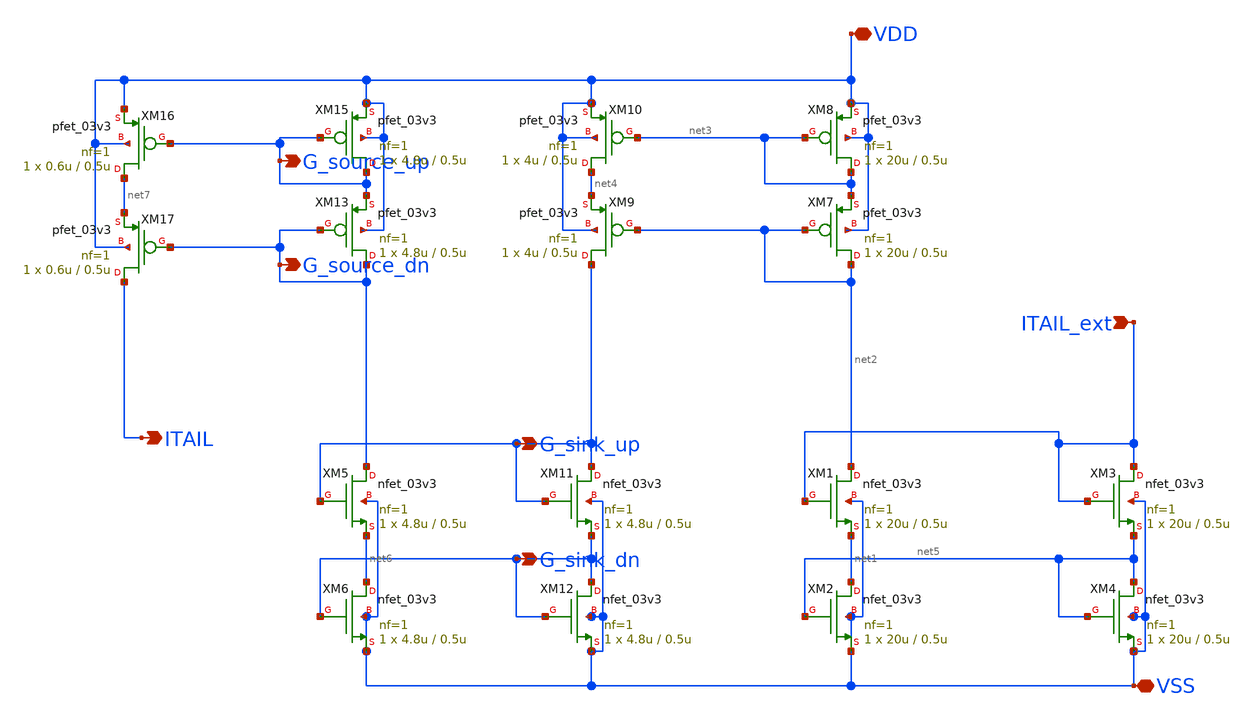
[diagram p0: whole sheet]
** sch_path: DAC_PAKISTAN_01/Pakistan1_Xschem/Current_Mirror_Top_s.sch
**.subckt Current_Mirror_Top_s ITAIL_ext VDD VSS G_source_up G_source_dn G_sink_up G_sink_dn ITAIL
*.ipin ITAIL_ext
*.iopin VDD
*.iopin VSS
*.opin G_source_up
*.opin G_source_dn
*.opin G_sink_up
*.opin G_sink_dn
*.opin ITAIL
XM1 net2 ITAIL_ext net1 VSS nfet_03v3 L=0.5u W=20u nf=1 ad='int((nf+1)/2) * W/nf * 0.18u' as='int((nf+2)/2) * W/nf * 0.18u'
+ pd='2*int((nf+1)/2) * (W/nf + 0.18u)' ps='2*int((nf+2)/2) * (W/nf + 0.18u)' nrd='0.18u / W' nrs='0.18u / W'
+ sa=0 sb=0 sd=0 m=1
XM2 net1 net5 VSS VSS nfet_03v3 L=0.5u W=20u nf=1 ad='int((nf+1)/2) * W/nf * 0.18u' as='int((nf+2)/2) * W/nf * 0.18u'
+ pd='2*int((nf+1)/2) * (W/nf + 0.18u)' ps='2*int((nf+2)/2) * (W/nf + 0.18u)' nrd='0.18u / W' nrs='0.18u / W'
+ sa=0 sb=0 sd=0 m=1
XM7 net2 net2 net3 VDD pfet_03v3 L=0.5u W=20u nf=1 ad='int((nf+1)/2) * W/nf * 0.18u' as='int((nf+2)/2) * W/nf * 0.18u'
+ pd='2*int((nf+1)/2) * (W/nf + 0.18u)' ps='2*int((nf+2)/2) * (W/nf + 0.18u)' nrd='0.18u / W' nrs='0.18u / W'
+ sa=0 sb=0 sd=0 m=1
XM8 net3 net3 VDD VDD pfet_03v3 L=0.5u W=20u nf=1 ad='int((nf+1)/2) * W/nf * 0.18u' as='int((nf+2)/2) * W/nf * 0.18u'
+ pd='2*int((nf+1)/2) * (W/nf + 0.18u)' ps='2*int((nf+2)/2) * (W/nf + 0.18u)' nrd='0.18u / W' nrs='0.18u / W'
+ sa=0 sb=0 sd=0 m=1
XM9 G_sink_up net2 net4 VDD pfet_03v3 L=0.5u W=4u nf=1 ad='int((nf+1)/2) * W/nf * 0.18u' as='int((nf+2)/2) * W/nf * 0.18u'
+ pd='2*int((nf+1)/2) * (W/nf + 0.18u)' ps='2*int((nf+2)/2) * (W/nf + 0.18u)' nrd='0.18u / W' nrs='0.18u / W'
+ sa=0 sb=0 sd=0 m=1
XM10 net4 net3 VDD VDD pfet_03v3 L=0.5u W=4u nf=1 ad='int((nf+1)/2) * W/nf * 0.18u' as='int((nf+2)/2) * W/nf * 0.18u'
+ pd='2*int((nf+1)/2) * (W/nf + 0.18u)' ps='2*int((nf+2)/2) * (W/nf + 0.18u)' nrd='0.18u / W' nrs='0.18u / W'
+ sa=0 sb=0 sd=0 m=1
XM11 G_sink_up G_sink_up G_sink_dn VSS nfet_03v3 L=0.5u W=4.8u nf=1 ad='int((nf+1)/2) * W/nf * 0.18u'
+ as='int((nf+2)/2) * W/nf * 0.18u' pd='2*int((nf+1)/2) * (W/nf + 0.18u)' ps='2*int((nf+2)/2) * (W/nf + 0.18u)'
+ nrd='0.18u / W' nrs='0.18u / W' sa=0 sb=0 sd=0 m=1
XM12 G_sink_dn G_sink_dn VSS VSS nfet_03v3 L=0.5u W=4.8u nf=1 ad='int((nf+1)/2) * W/nf * 0.18u' as='int((nf+2)/2) * W/nf * 0.18u'
+ pd='2*int((nf+1)/2) * (W/nf + 0.18u)' ps='2*int((nf+2)/2) * (W/nf + 0.18u)' nrd='0.18u / W' nrs='0.18u / W'
+ sa=0 sb=0 sd=0 m=1
XM3 ITAIL_ext ITAIL_ext net5 VSS nfet_03v3 L=0.5u W=20u nf=1 ad='int((nf+1)/2) * W/nf * 0.18u' as='int((nf+2)/2) * W/nf * 0.18u'
+ pd='2*int((nf+1)/2) * (W/nf + 0.18u)' ps='2*int((nf+2)/2) * (W/nf + 0.18u)' nrd='0.18u / W' nrs='0.18u / W'
+ sa=0 sb=0 sd=0 m=1
XM4 net5 net5 VSS VSS nfet_03v3 L=0.5u W=20u nf=1 ad='int((nf+1)/2) * W/nf * 0.18u' as='int((nf+2)/2) * W/nf * 0.18u'
+ pd='2*int((nf+1)/2) * (W/nf + 0.18u)' ps='2*int((nf+2)/2) * (W/nf + 0.18u)' nrd='0.18u / W' nrs='0.18u / W'
+ sa=0 sb=0 sd=0 m=1
XM5 G_source_dn G_sink_up net6 VSS nfet_03v3 L=0.5u W=4.8u nf=1 ad='int((nf+1)/2) * W/nf * 0.18u' as='int((nf+2)/2) * W/nf * 0.18u'
+ pd='2*int((nf+1)/2) * (W/nf + 0.18u)' ps='2*int((nf+2)/2) * (W/nf + 0.18u)' nrd='0.18u / W' nrs='0.18u / W'
+ sa=0 sb=0 sd=0 m=1
XM6 net6 G_sink_dn VSS VSS nfet_03v3 L=0.5u W=4.8u nf=1 ad='int((nf+1)/2) * W/nf * 0.18u' as='int((nf+2)/2) * W/nf * 0.18u'
+ pd='2*int((nf+1)/2) * (W/nf + 0.18u)' ps='2*int((nf+2)/2) * (W/nf + 0.18u)' nrd='0.18u / W' nrs='0.18u / W'
+ sa=0 sb=0 sd=0 m=1
XM13 G_source_dn G_source_dn G_source_up VDD pfet_03v3 L=0.5u W=4.8u nf=1 ad='int((nf+1)/2) * W/nf * 0.18u'
+ as='int((nf+2)/2) * W/nf * 0.18u' pd='2*int((nf+1)/2) * (W/nf + 0.18u)' ps='2*int((nf+2)/2) * (W/nf + 0.18u)'
+ nrd='0.18u / W' nrs='0.18u / W' sa=0 sb=0 sd=0 m=1
XM15 G_source_up G_source_up VDD VDD pfet_03v3 L=0.5u W=4.8u nf=1 ad='int((nf+1)/2) * W/nf * 0.18u' as='int((nf+2)/2) * W/nf * 0.18u'
+ pd='2*int((nf+1)/2) * (W/nf + 0.18u)' ps='2*int((nf+2)/2) * (W/nf + 0.18u)' nrd='0.18u / W' nrs='0.18u / W'
+ sa=0 sb=0 sd=0 m=1
XM16 net7 G_source_up VDD VDD pfet_03v3 L=0.5u W=0.6u nf=1 ad='int((nf+1)/2) * W/nf * 0.18u' as='int((nf+2)/2) * W/nf * 0.18u'
+ pd='2*int((nf+1)/2) * (W/nf + 0.18u)' ps='2*int((nf+2)/2) * (W/nf + 0.18u)' nrd='0.18u / W' nrs='0.18u / W'
+ sa=0 sb=0 sd=0 m=1
XM17 ITAIL G_source_dn net7 VDD pfet_03v3 L=0.5u W=0.6u nf=1 ad='int((nf+1)/2) * W/nf * 0.18u' as='int((nf+2)/2) * W/nf * 0.18u'
+ pd='2*int((nf+1)/2) * (W/nf + 0.18u)' ps='2*int((nf+2)/2) * (W/nf + 0.18u)' nrd='0.18u / W' nrs='0.18u / W'
+ sa=0 sb=0 sd=0 m=1
**.ends
.end
